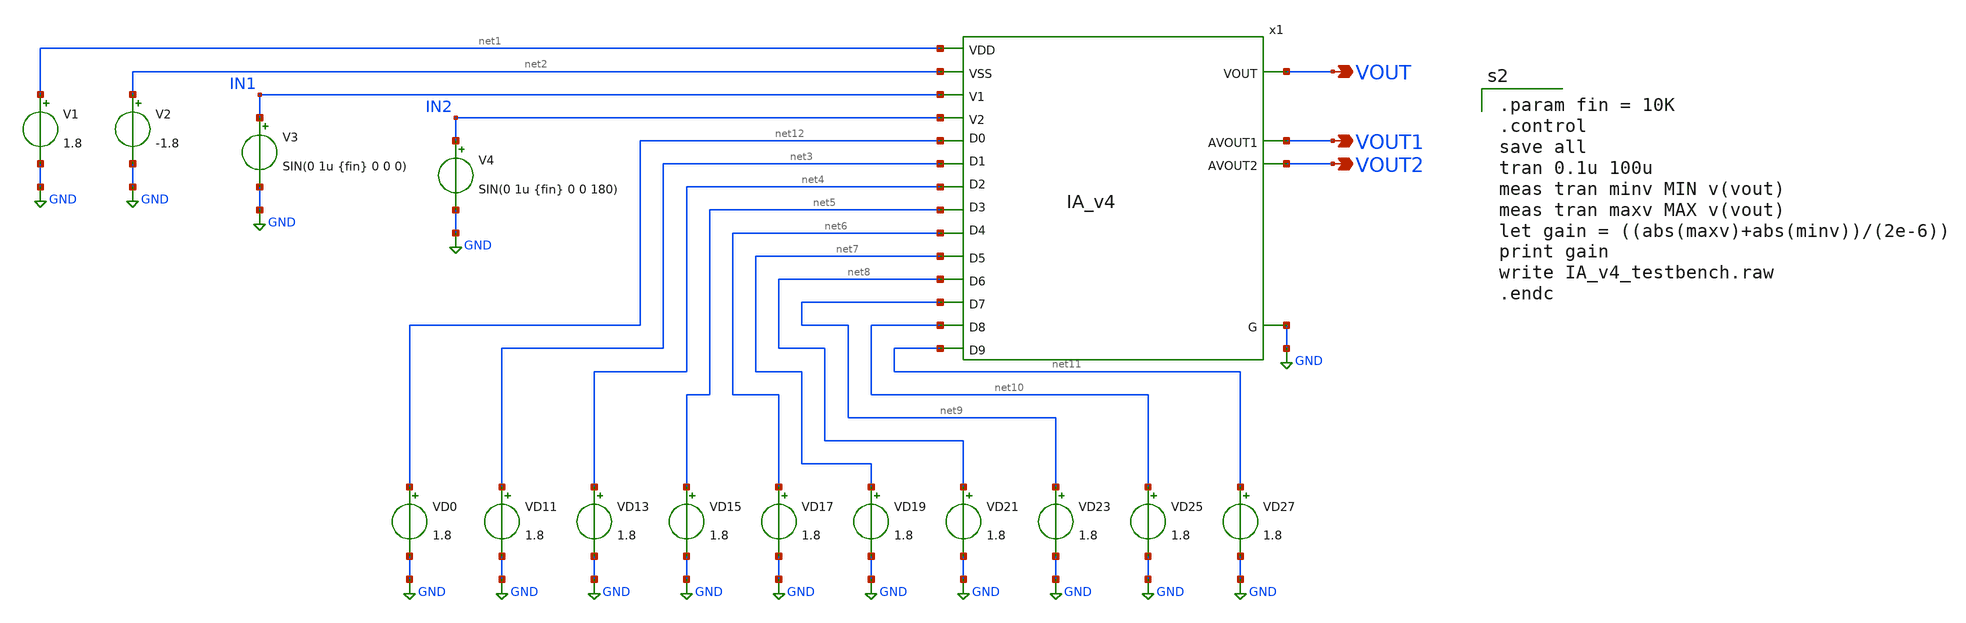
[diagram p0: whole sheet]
** sch_path: xschem/IA_v4_testbench.sch
**.subckt IA_v4_testbench VOUT VOUT1 VOUT2
*.opin VOUT
*.opin VOUT1
*.opin VOUT2
V1 net1 GND 1.8
V2 net2 GND -1.8
V3 IN1 GND SIN(0 1u {fin} 0 0 0)
V4 IN2 GND SIN(0 1u {fin} 0 0 180)
VD0 net12 GND 1.8
VD11 net3 GND 1.8
VD13 net4 GND 1.8
VD15 net5 GND 1.8
VD17 net6 GND 1.8
VD19 net7 GND 1.8
VD21 net8 GND 1.8
VD23 net9 GND 1.8
VD25 net10 GND 1.8
VD27 net11 GND 1.8
x1 net1 net2 GND IN1 IN2 net12 net3 net4 net5 net6 net7 net8 net9 net10 net11 VOUT1 VOUT2 VOUT IA_v4
**** begin user architecture code

.param fin = 10K
.control
save all
tran 0.1u 100u
meas tran minv MIN v(vout)
meas tran maxv MAX v(vout)
let gain = ((abs(maxv)+abs(minv))/(2e-6))
print gain
write IA_v4_testbench.raw
.endc

.lib $::SKYWATER_MODELS/sky130.lib.spice tt
**** end user architecture code
**.ends
.GLOBAL GND
.end
